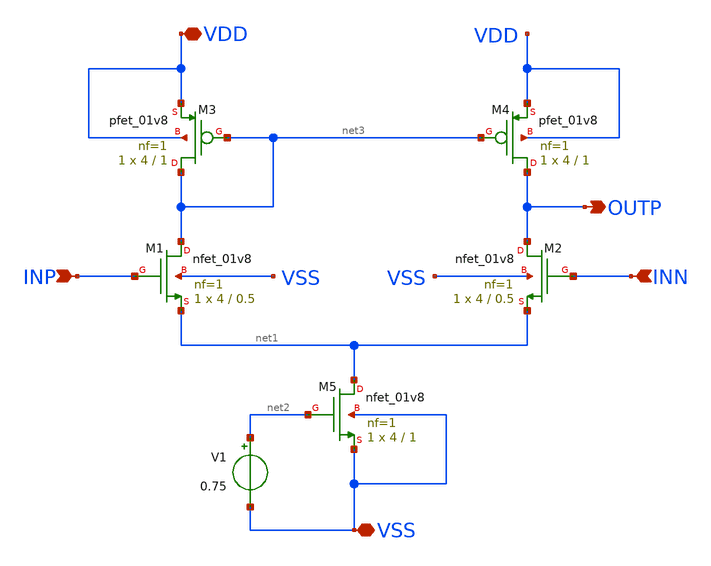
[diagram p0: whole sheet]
** sch_path: circuits/ota5t_gui_copy/source/example_ota_5t.sch
**.subckt example_ota_5t INP INN OUTP VDD VSS
*.ipin INP
*.ipin INN
*.opin OUTP
*.iopin VDD
*.iopin VSS
XM3 net3 net3 VDD VDD sky130_fd_pr__pfet_01v8 L=1 W=4 nf=1 ad='int((nf+1)/2) * W/nf * 0.29' as='int((nf+2)/2) * W/nf * 0.29'
+ pd='2*int((nf+1)/2) * (W/nf + 0.29)' ps='2*int((nf+2)/2) * (W/nf + 0.29)' nrd='0.29 / W' nrs='0.29 / W'
+ sa=0 sb=0 sd=0 mult=1 m=1
XM4 OUTP net3 VDD VDD sky130_fd_pr__pfet_01v8 L=1 W=4 nf=1 ad='int((nf+1)/2) * W/nf * 0.29' as='int((nf+2)/2) * W/nf * 0.29'
+ pd='2*int((nf+1)/2) * (W/nf + 0.29)' ps='2*int((nf+2)/2) * (W/nf + 0.29)' nrd='0.29 / W' nrs='0.29 / W'
+ sa=0 sb=0 sd=0 mult=1 m=1
XM1 net3 INP net1 VSS sky130_fd_pr__nfet_01v8 L=0.5 W=4 nf=1 ad='int((1 + 1)/2) * 4 / 1 * 0.29' as='int((1 + 2)/2) * 4 / 1 * 0.29'
+ pd='2*int((1 + 1)/2) * (4 / 1 + 0.29)' ps='2*int((1 + 2)/2) * (4 / 1 + 0.29)' nrd='0.29 / 4 ' nrs='0.29 / 4 '
+ sa=0 sb=0 sd=0 mult=1 m=1
XM2 OUTP INN net1 VSS sky130_fd_pr__nfet_01v8 L=0.5 W=4 nf=1 ad='int((1 + 1)/2) * 4 / 1 * 0.29' as='int((1 + 2)/2) * 4 / 1 * 0.29'
+ pd='2*int((1 + 1)/2) * (4 / 1 + 0.29)' ps='2*int((1 + 2)/2) * (4 / 1 + 0.29)' nrd='0.29 / 4 ' nrs='0.29 / 4 '
+ sa=0 sb=0 sd=0 mult=1 m=1
XM5 net1 net2 VSS VSS sky130_fd_pr__nfet_01v8 L=1 W=4 nf=1 ad='int((1 + 1)/2) * 4 / 1 * 0.29' as='int((1 + 2)/2) * 4 / 1 * 0.29'
+ pd='2*int((1 + 1)/2) * (4 / 1 + 0.29)' ps='2*int((1 + 2)/2) * (4 / 1 + 0.29)' nrd='0.29 / 4 ' nrs='0.29 / 4 '
+ sa=0 sb=0 sd=0 mult=1 m=1
V1 net2 VSS 0.75
**.ends
.end
